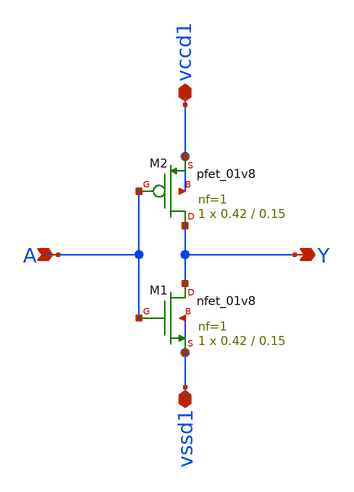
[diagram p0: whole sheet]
** sch_path: mag/final_designs/inv_LV.sch
**.subckt inv_LV vccd1 vssd1 A Y
*.iopin vccd1
*.iopin vssd1
*.ipin A
*.opin Y
XM1 Y A vssd1 vssd1 sky130_fd_pr__nfet_01v8 L=0.15 W=0.42 nf=1 ad='int((nf+1)/2) * W/nf * 0.29' as='int((nf+2)/2) * W/nf * 0.29'
+ pd='2*int((nf+1)/2) * (W/nf + 0.29)' ps='2*int((nf+2)/2) * (W/nf + 0.29)' nrd='0.29 / W' nrs='0.29 / W'
+ sa=0 sb=0 sd=0 mult=1 m=1
XM2 Y A vccd1 vccd1 sky130_fd_pr__pfet_01v8 L=0.15 W=0.42 nf=1 ad='int((nf+1)/2) * W/nf * 0.29' as='int((nf+2)/2) * W/nf * 0.29'
+ pd='2*int((nf+1)/2) * (W/nf + 0.29)' ps='2*int((nf+2)/2) * (W/nf + 0.29)' nrd='0.29 / W' nrs='0.29 / W'
+ sa=0 sb=0 sd=0 mult=1 m=1
**.ends
.end
